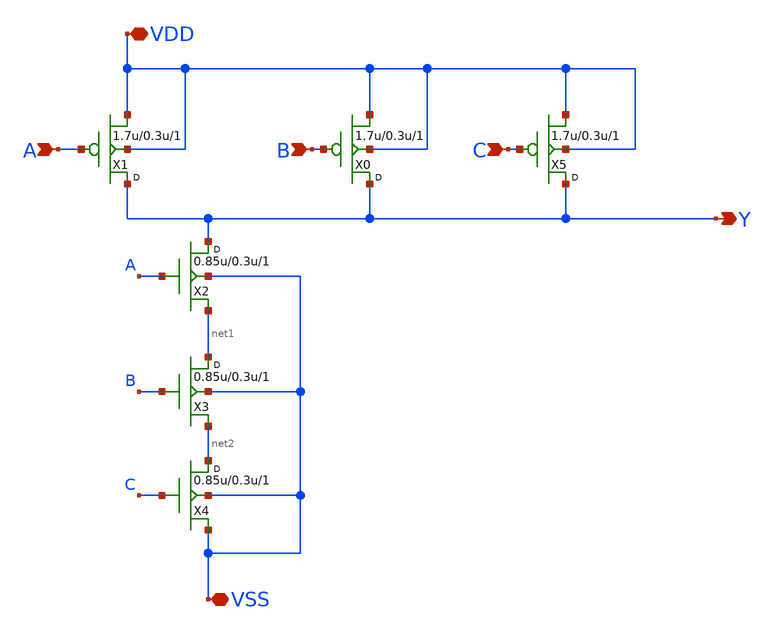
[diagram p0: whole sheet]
** sch_path: designs/libs/core_digital/gf180mcu_osu_sc_gp9t3v3/cells/nand3/gf180mcu_osu_sc_gp9t3v3__nand3_1.sch
**.subckt gf180mcu_osu_sc_gp9t3v3__nand3_1 A B Y C VDD VSS
*.ipin A
*.ipin B
*.opin Y
*.ipin C
*.iopin VDD
*.iopin VSS
X1 Y A VDD VDD pfet_03v3 w=1.7u l=0.3u m=1
X0 Y B VDD VDD pfet_03v3 w=1.7u l=0.3u m=1
X2 Y A net1 VSS nfet_03v3 w=0.85u l=0.3u m=1
X3 net1 B net2 VSS nfet_03v3 w=0.85u l=0.3u m=1
X4 net2 C VSS VSS nfet_03v3 w=0.85u l=0.3u m=1
X5 Y C VDD VDD pfet_03v3 w=1.7u l=0.3u m=1
**.ends
.end
